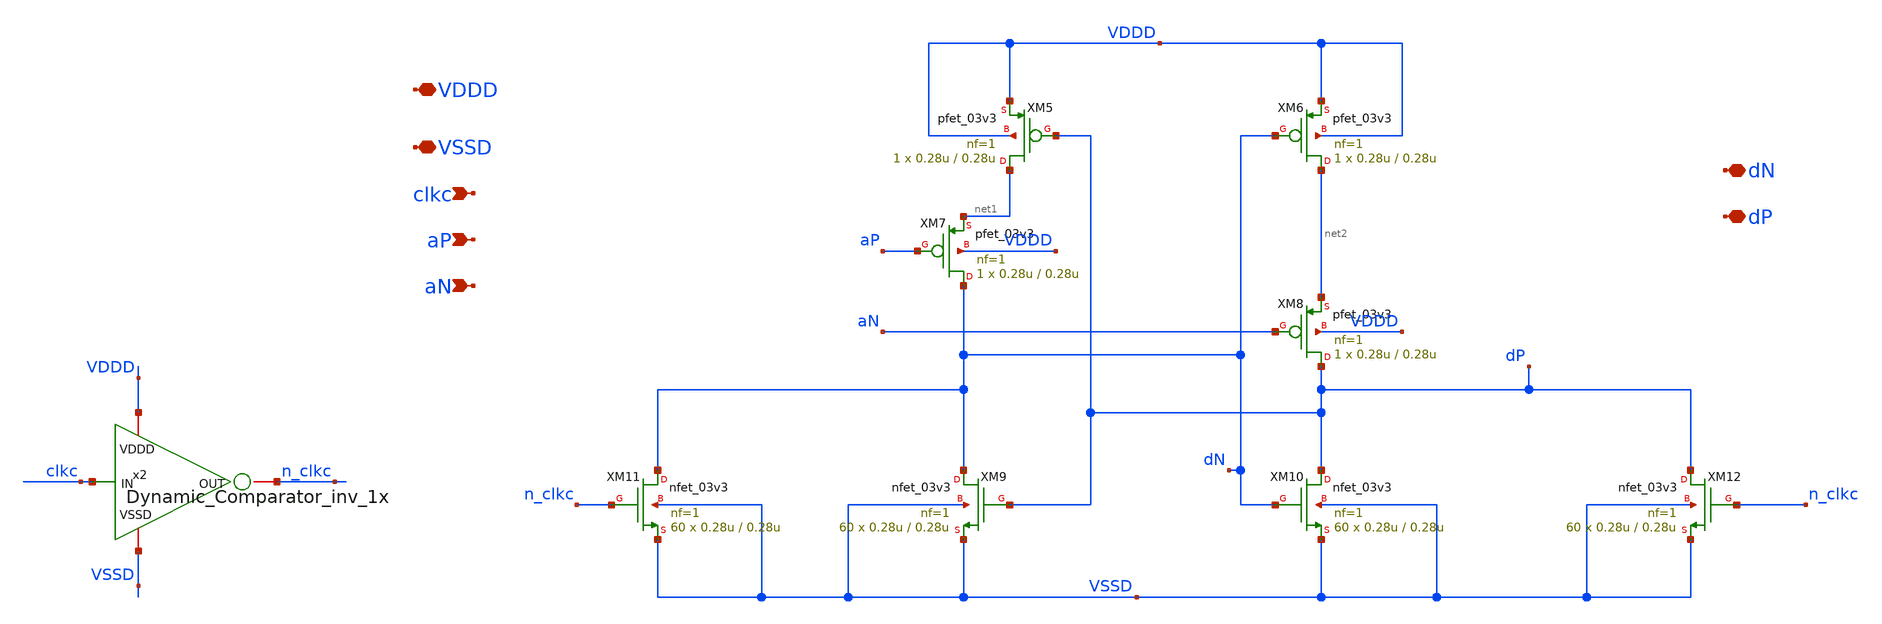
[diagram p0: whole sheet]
** sch_path: SAR_ADC/blocks/Dynamic_Comparator/Dynamic_Comparator_latch.sch
**.subckt Dynamic_Comparator_latch VDDD VSSD clkc aP aN dN dP
*.iopin VDDD
*.iopin VSSD
*.ipin clkc
*.ipin aP
*.ipin aN
*.iopin dN
*.iopin dP
XM5 net1 dP VDDD VDDD pfet_03v3 L=0.28u W=0.28u nf=1 ad='int((nf+1)/2) * W/nf * 0.18u' as='int((nf+2)/2) * W/nf * 0.18u'
+ pd='2*int((nf+1)/2) * (W/nf + 0.18u)' ps='2*int((nf+2)/2) * (W/nf + 0.18u)' nrd='0.18u / W' nrs='0.18u / W'
+ sa=0 sb=0 sd=0 m=1
XM6 net2 dN VDDD VDDD pfet_03v3 L=0.28u W=0.28u nf=1 ad='int((nf+1)/2) * W/nf * 0.18u' as='int((nf+2)/2) * W/nf * 0.18u'
+ pd='2*int((nf+1)/2) * (W/nf + 0.18u)' ps='2*int((nf+2)/2) * (W/nf + 0.18u)' nrd='0.18u / W' nrs='0.18u / W'
+ sa=0 sb=0 sd=0 m=1
XM7 dN aP net1 VDDD pfet_03v3 L=0.28u W=0.28u nf=1 ad='int((nf+1)/2) * W/nf * 0.18u' as='int((nf+2)/2) * W/nf * 0.18u'
+ pd='2*int((nf+1)/2) * (W/nf + 0.18u)' ps='2*int((nf+2)/2) * (W/nf + 0.18u)' nrd='0.18u / W' nrs='0.18u / W'
+ sa=0 sb=0 sd=0 m=1
XM8 dP aN net2 VDDD pfet_03v3 L=0.28u W=0.28u nf=1 ad='int((nf+1)/2) * W/nf * 0.18u' as='int((nf+2)/2) * W/nf * 0.18u'
+ pd='2*int((nf+1)/2) * (W/nf + 0.18u)' ps='2*int((nf+2)/2) * (W/nf + 0.18u)' nrd='0.18u / W' nrs='0.18u / W'
+ sa=0 sb=0 sd=0 m=1
XM9 dN dP VSSD VSSD nfet_03v3 L=0.28u W=0.28u nf=1 ad='int((nf+1)/2) * W/nf * 0.18u' as='int((nf+2)/2) * W/nf * 0.18u'
+ pd='2*int((nf+1)/2) * (W/nf + 0.18u)' ps='2*int((nf+2)/2) * (W/nf + 0.18u)' nrd='0.18u / W' nrs='0.18u / W'
+ sa=0 sb=0 sd=0 m=60
XM10 dP dN VSSD VSSD nfet_03v3 L=0.28u W=0.28u nf=1 ad='int((nf+1)/2) * W/nf * 0.18u' as='int((nf+2)/2) * W/nf * 0.18u'
+ pd='2*int((nf+1)/2) * (W/nf + 0.18u)' ps='2*int((nf+2)/2) * (W/nf + 0.18u)' nrd='0.18u / W' nrs='0.18u / W'
+ sa=0 sb=0 sd=0 m=60
XM11 dN n_clkc VSSD VSSD nfet_03v3 L=0.28u W=0.28u nf=1 ad='int((nf+1)/2) * W/nf * 0.18u' as='int((nf+2)/2) * W/nf * 0.18u'
+ pd='2*int((nf+1)/2) * (W/nf + 0.18u)' ps='2*int((nf+2)/2) * (W/nf + 0.18u)' nrd='0.18u / W' nrs='0.18u / W'
+ sa=0 sb=0 sd=0 m=60
XM12 dP n_clkc VSSD VSSD nfet_03v3 L=0.28u W=0.28u nf=1 ad='int((nf+1)/2) * W/nf * 0.18u' as='int((nf+2)/2) * W/nf * 0.18u'
+ pd='2*int((nf+1)/2) * (W/nf + 0.18u)' ps='2*int((nf+2)/2) * (W/nf + 0.18u)' nrd='0.18u / W' nrs='0.18u / W'
+ sa=0 sb=0 sd=0 m=60
x2 VDDD VSSD n_clkc clkc Dynamic_Comparator_inv_1x
**.ends

* expanding   symbol:
*+  /home/electrica/Documents/gf180_projects/gf180_work/PICO_contest/Dynamic_Comparator/Dynamic_Comparator_inv_1x.sym # of pins=4
** sym_path: SAR_ADC/Dynamic_Comparator/xschem/Dynamic_Comparator_inv_1x.sym
** sch_path: SAR_ADC/Dynamic_Comparator/xschem/Dynamic_Comparator_inv_1x.sch
.subckt Dynamic_Comparator_inv_1x VDDD VSSD OUT IN
*.iopin VDDD
*.iopin VSSD
*.ipin IN
*.iopin OUT
XM1 OUT IN VSSD VSSD nfet_03v3 L=0.28u W=1.56u nf=1 ad='int((nf+1)/2) * W/nf * 0.18u' as='int((nf+2)/2) * W/nf * 0.18u'
+ pd='2*int((nf+1)/2) * (W/nf + 0.18u)' ps='2*int((nf+2)/2) * (W/nf + 0.18u)' nrd='0.18u / W' nrs='0.18u / W'
+ sa=0 sb=0 sd=0 m=1
XM2 OUT IN VDDD VDDD pfet_03v3 L=0.28u W=3.9u nf=1 ad='int((nf+1)/2) * W/nf * 0.18u' as='int((nf+2)/2) * W/nf * 0.18u'
+ pd='2*int((nf+1)/2) * (W/nf + 0.18u)' ps='2*int((nf+2)/2) * (W/nf + 0.18u)' nrd='0.18u / W' nrs='0.18u / W'
+ sa=0 sb=0 sd=0 m=1
.ends

.end
